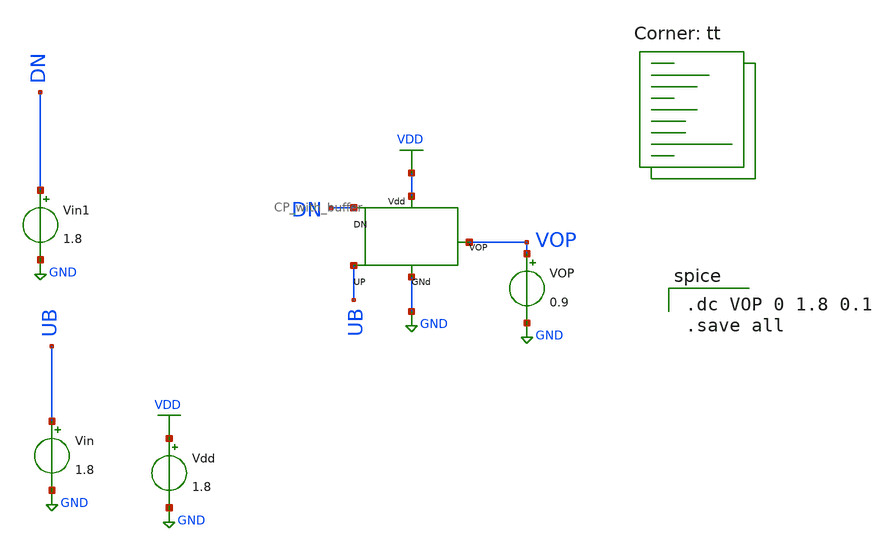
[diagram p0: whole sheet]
** sch_path: pll/pfd_cp_lf_lib/charge_pump_second_design_tb/xschem/cp_second_design_tb.sch
**.subckt cp_second_design_tb
Vdd VDD GND 1.8
Vin UB GND 1.8
Vin1 DN GND 1.8
VOP VOP GND 0.9
X1 DN VOP UB VDD GND CP_with_buffer
**** begin user architecture code
.lib $::SKYWATER_MODELS/sky130.lib.spice tt

.dc VOP 0 1.8 0.1
.save all

**** end user architecture code
**.ends
.GLOBAL GND
.GLOBAL VDD
.end
